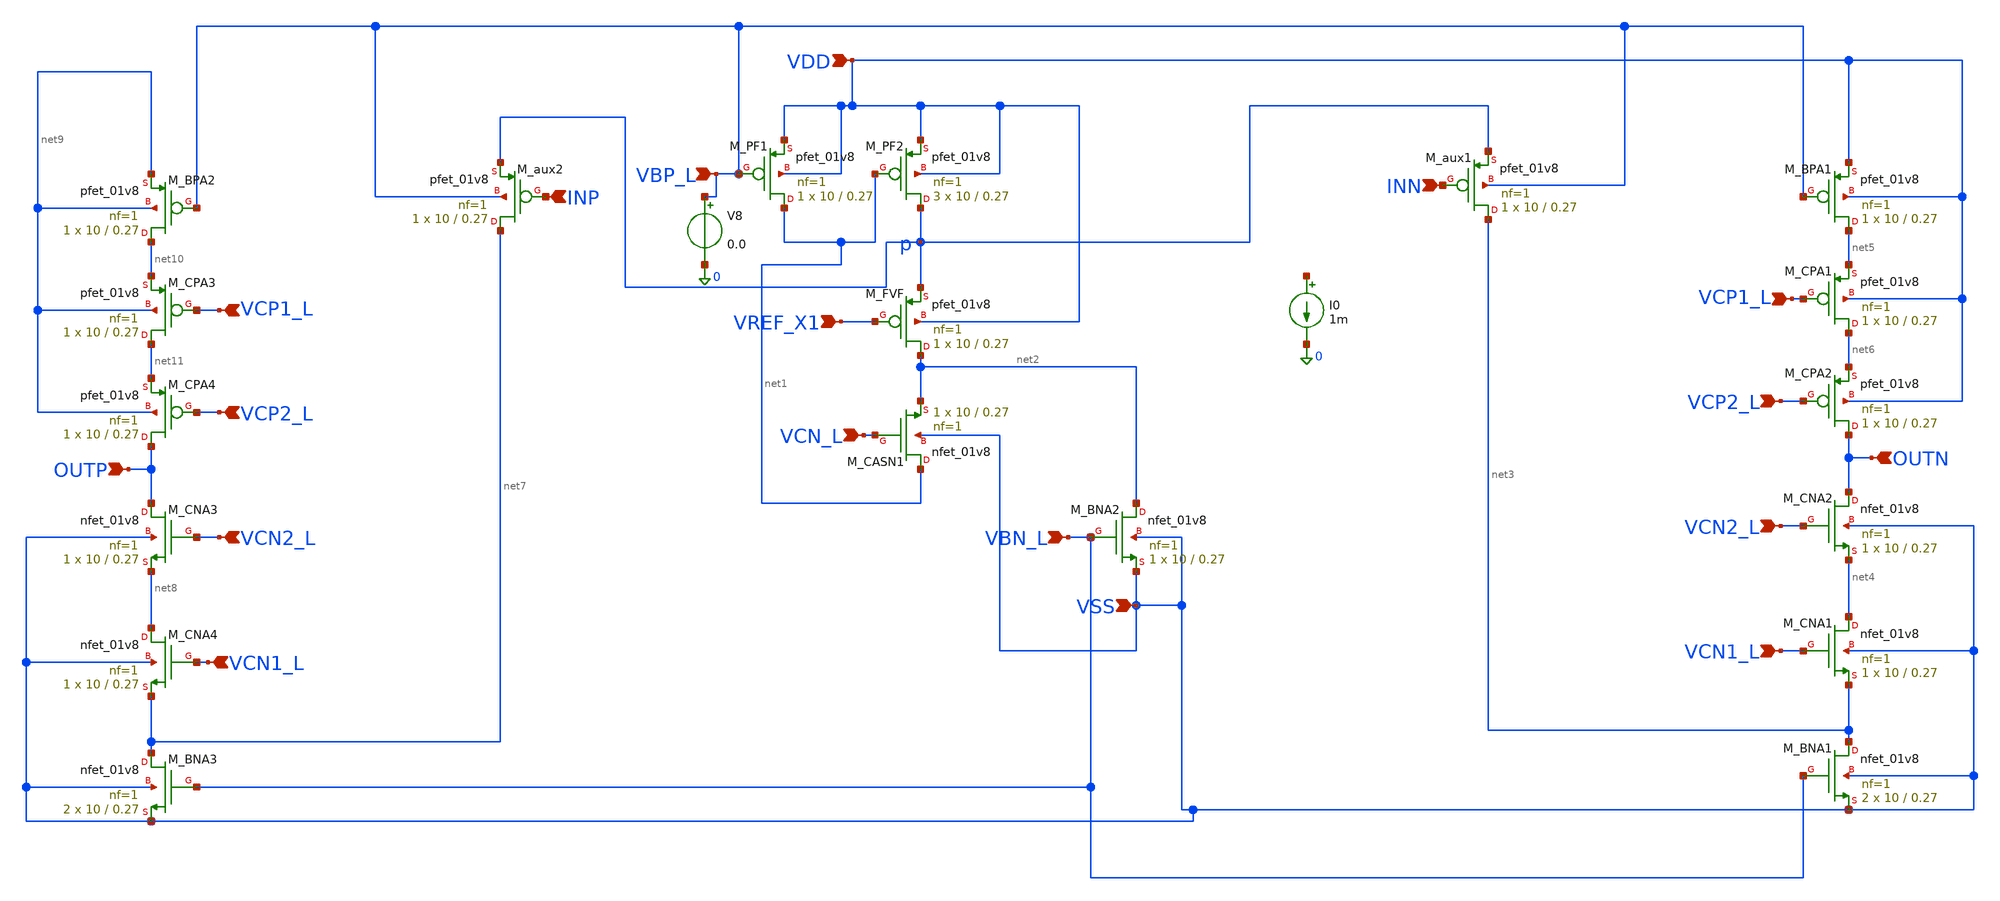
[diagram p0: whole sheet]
** sch_path: auxp.sch
**.subckt auxp VSS VDD VBN_L VCN_L VBP_L VREF_X1 INN OUTN VCP1_L VCP2_L VCN1_L VCN2_L INP OUTP
*+ VCP1_L VCP2_L VCN1_L VCN2_L
*.ipin VSS
*.ipin VDD
*.ipin VBN_L
*.ipin VCN_L
*.ipin VBP_L
*.ipin VREF_X1
*.ipin INN
*.ipin OUTN
*.ipin VCP1_L
*.ipin VCP2_L
*.ipin VCN1_L
*.ipin VCN2_L
*.ipin INP
*.ipin OUTP
*.ipin VCP1_L
*.ipin VCP2_L
*.ipin VCN1_L
*.ipin VCN2_L
XM_BNA2 net2 VBN_L VSS VSS sky130_fd_pr__nfet_01v8 L=0.27 W=10 nf=1 ad='int((1 + 1)/2) * 10 / 1 * 0.29'
+ as='int((1 + 2)/2) * 10 / 1 * 0.29' pd='2*int((1 + 1)/2) * (10 / 1 + 0.29)' ps='2*int((1 + 2)/2) * (10 / 1 + 0.29)'
+ nrd='0.29 / 10 ' nrs='0.29 / 10 ' sa=0 sb=0 sd=0 mult=1 m=1
XM_FVF net2 VREF_X1 p VDD sky130_fd_pr__pfet_01v8 L=0.27 W=10 nf=1 ad='int((1 + 1)/2) * 10 / 1 * 0.29'
+ as='int((1 + 2)/2) * 10 / 1 * 0.29' pd='2*int((1 + 1)/2) * (10 / 1 + 0.29)' ps='2*int((1 + 2)/2) * (10 / 1 + 0.29)'
+ nrd='0.29 / 10 ' nrs='0.29 / 10 ' sa=0 sb=0 sd=0 mult=1 m=1
XM_PF1 net1 VBP_L VDD VDD sky130_fd_pr__pfet_01v8 L=0.27 W=10 nf=1 ad='int((1 + 1)/2) * 10 / 1 * 0.29'
+ as='int((1 + 2)/2) * 10 / 1 * 0.29' pd='2*int((1 + 1)/2) * (10 / 1 + 0.29)' ps='2*int((1 + 2)/2) * (10 / 1 + 0.29)'
+ nrd='0.29 / 10 ' nrs='0.29 / 10 ' sa=0 sb=0 sd=0 mult=1 m=1
XM_PF2 p net1 VDD VDD sky130_fd_pr__pfet_01v8 L=0.27 W=10 nf=1 ad='int((1 + 1)/2) * 10 / 1 * 0.29' as='int((1 + 2)/2) * 10 / 1 * 0.29'
+ pd='2*int((1 + 1)/2) * (10 / 1 + 0.29)' ps='2*int((1 + 2)/2) * (10 / 1 + 0.29)' nrd='0.29 / 10 ' nrs='0.29 / 10 '
+ sa=0 sb=0 sd=0 mult=3 m=3
XM_CASN1 net1 VCN_L net2 VSS sky130_fd_pr__nfet_01v8 L=0.27 W=10 nf=1 ad='int((1 + 1)/2) * 10 / 1 * 0.29'
+ as='int((1 + 2)/2) * 10 / 1 * 0.29' pd='2*int((1 + 1)/2) * (10 / 1 + 0.29)' ps='2*int((1 + 2)/2) * (10 / 1 + 0.29)'
+ nrd='0.29 / 10 ' nrs='0.29 / 10 ' sa=0 sb=0 sd=0 mult=1 m=1
I0 net12 0 1m
XM_aux1 net3 INN p VBP_L sky130_fd_pr__pfet_01v8 L=0.27 W=10 nf=1 ad='int((1 + 1)/2) * 10 / 1 * 0.29'
+ as='int((1 + 2)/2) * 10 / 1 * 0.29' pd='2*int((1 + 1)/2) * (10 / 1 + 0.29)' ps='2*int((1 + 2)/2) * (10 / 1 + 0.29)'
+ nrd='0.29 / 10 ' nrs='0.29 / 10 ' sa=0 sb=0 sd=0 mult=1 m=1
XM_BPA1 net5 VBP_L VDD VDD sky130_fd_pr__pfet_01v8 L=0.27 W=10 nf=1 ad='int((1 + 1)/2) * 10 / 1 * 0.29'
+ as='int((1 + 2)/2) * 10 / 1 * 0.29' pd='2*int((1 + 1)/2) * (10 / 1 + 0.29)' ps='2*int((1 + 2)/2) * (10 / 1 + 0.29)'
+ nrd='0.29 / 10 ' nrs='0.29 / 10 ' sa=0 sb=0 sd=0 mult=1 m=1
XM_CPA1 net6 VCP1_L net5 VDD sky130_fd_pr__pfet_01v8 L=0.27 W=10 nf=1 ad='int((1 + 1)/2) * 10 / 1 * 0.29'
+ as='int((1 + 2)/2) * 10 / 1 * 0.29' pd='2*int((1 + 1)/2) * (10 / 1 + 0.29)' ps='2*int((1 + 2)/2) * (10 / 1 + 0.29)'
+ nrd='0.29 / 10 ' nrs='0.29 / 10 ' sa=0 sb=0 sd=0 mult=1 m=1
XM_CPA2 OUTN VCP2_L net6 VDD sky130_fd_pr__pfet_01v8 L=0.27 W=10 nf=1 ad='int((1 + 1)/2) * 10 / 1 * 0.29'
+ as='int((1 + 2)/2) * 10 / 1 * 0.29' pd='2*int((1 + 1)/2) * (10 / 1 + 0.29)' ps='2*int((1 + 2)/2) * (10 / 1 + 0.29)'
+ nrd='0.29 / 10 ' nrs='0.29 / 10 ' sa=0 sb=0 sd=0 mult=1 m=1
XM_CNA2 OUTN VCN2_L net4 VSS sky130_fd_pr__nfet_01v8 L=0.27 W=10 nf=1 ad='int((1 + 1)/2) * 10 / 1 * 0.29'
+ as='int((1 + 2)/2) * 10 / 1 * 0.29' pd='2*int((1 + 1)/2) * (10 / 1 + 0.29)' ps='2*int((1 + 2)/2) * (10 / 1 + 0.29)'
+ nrd='0.29 / 10 ' nrs='0.29 / 10 ' sa=0 sb=0 sd=0 mult=1 m=1
XM_CNA1 net4 VCN1_L net3 VSS sky130_fd_pr__nfet_01v8 L=0.27 W=10 nf=1 ad='int((1 + 1)/2) * 10 / 1 * 0.29'
+ as='int((1 + 2)/2) * 10 / 1 * 0.29' pd='2*int((1 + 1)/2) * (10 / 1 + 0.29)' ps='2*int((1 + 2)/2) * (10 / 1 + 0.29)'
+ nrd='0.29 / 10 ' nrs='0.29 / 10 ' sa=0 sb=0 sd=0 mult=1 m=1
XM_BNA1 net3 VBN_L VSS VSS sky130_fd_pr__nfet_01v8 L=0.27 W=10 nf=1 ad='int((1 + 1)/2) * 10 / 1 * 0.29'
+ as='int((1 + 2)/2) * 10 / 1 * 0.29' pd='2*int((1 + 1)/2) * (10 / 1 + 0.29)' ps='2*int((1 + 2)/2) * (10 / 1 + 0.29)'
+ nrd='0.29 / 10 ' nrs='0.29 / 10 ' sa=0 sb=0 sd=0 mult=2 m=2
XM_aux2 net7 INP p VBP_L sky130_fd_pr__pfet_01v8 L=0.27 W=10 nf=1 ad='int((1 + 1)/2) * 10 / 1 * 0.29'
+ as='int((1 + 2)/2) * 10 / 1 * 0.29' pd='2*int((1 + 1)/2) * (10 / 1 + 0.29)' ps='2*int((1 + 2)/2) * (10 / 1 + 0.29)'
+ nrd='0.29 / 10 ' nrs='0.29 / 10 ' sa=0 sb=0 sd=0 mult=1 m=1
XM_BPA2 net10 VBP_L net9 net9 sky130_fd_pr__pfet_01v8 L=0.27 W=10 nf=1 ad='int((1 + 1)/2) * 10 / 1 * 0.29'
+ as='int((1 + 2)/2) * 10 / 1 * 0.29' pd='2*int((1 + 1)/2) * (10 / 1 + 0.29)' ps='2*int((1 + 2)/2) * (10 / 1 + 0.29)'
+ nrd='0.29 / 10 ' nrs='0.29 / 10 ' sa=0 sb=0 sd=0 mult=1 m=1
XM_CPA3 net11 VCP1_L net10 net9 sky130_fd_pr__pfet_01v8 L=0.27 W=10 nf=1 ad='int((1 + 1)/2) * 10 / 1 * 0.29'
+ as='int((1 + 2)/2) * 10 / 1 * 0.29' pd='2*int((1 + 1)/2) * (10 / 1 + 0.29)' ps='2*int((1 + 2)/2) * (10 / 1 + 0.29)'
+ nrd='0.29 / 10 ' nrs='0.29 / 10 ' sa=0 sb=0 sd=0 mult=1 m=1
XM_CPA4 OUTP VCP2_L net11 net9 sky130_fd_pr__pfet_01v8 L=0.27 W=10 nf=1 ad='int((1 + 1)/2) * 10 / 1 * 0.29'
+ as='int((1 + 2)/2) * 10 / 1 * 0.29' pd='2*int((1 + 1)/2) * (10 / 1 + 0.29)' ps='2*int((1 + 2)/2) * (10 / 1 + 0.29)'
+ nrd='0.29 / 10 ' nrs='0.29 / 10 ' sa=0 sb=0 sd=0 mult=1 m=1
XM_CNA3 OUTP VCN2_L net8 VSS sky130_fd_pr__nfet_01v8 L=0.27 W=10 nf=1 ad='int((1 + 1)/2) * 10 / 1 * 0.29'
+ as='int((1 + 2)/2) * 10 / 1 * 0.29' pd='2*int((1 + 1)/2) * (10 / 1 + 0.29)' ps='2*int((1 + 2)/2) * (10 / 1 + 0.29)'
+ nrd='0.29 / 10 ' nrs='0.29 / 10 ' sa=0 sb=0 sd=0 mult=1 m=1
XM_CNA4 net8 VCN1_L net7 VSS sky130_fd_pr__nfet_01v8 L=0.27 W=10 nf=1 ad='int((1 + 1)/2) * 10 / 1 * 0.29'
+ as='int((1 + 2)/2) * 10 / 1 * 0.29' pd='2*int((1 + 1)/2) * (10 / 1 + 0.29)' ps='2*int((1 + 2)/2) * (10 / 1 + 0.29)'
+ nrd='0.29 / 10 ' nrs='0.29 / 10 ' sa=0 sb=0 sd=0 mult=1 m=1
XM_BNA3 net7 VBN_L VSS VSS sky130_fd_pr__nfet_01v8 L=0.27 W=10 nf=1 ad='int((1 + 1)/2) * 10 / 1 * 0.29'
+ as='int((1 + 2)/2) * 10 / 1 * 0.29' pd='2*int((1 + 1)/2) * (10 / 1 + 0.29)' ps='2*int((1 + 2)/2) * (10 / 1 + 0.29)'
+ nrd='0.29 / 10 ' nrs='0.29 / 10 ' sa=0 sb=0 sd=0 mult=2 m=2
V8 VBP_L 0 0.0
**.ends
.end
